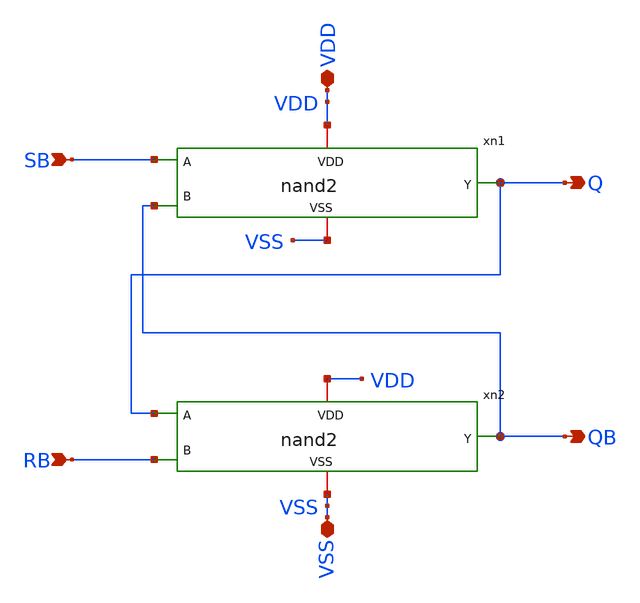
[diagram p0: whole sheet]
** sch_path: schematics/sr_latch.sch
**.subckt sr_latch VDD VSS SB RB Q QB
*.iopin VDD
*.iopin VSS
*.ipin SB
*.ipin RB
*.opin Q
*.opin QB
xn1 VDD SB Q QB VSS nand2
xn2 VDD Q QB RB VSS nand2
**.ends
.end
